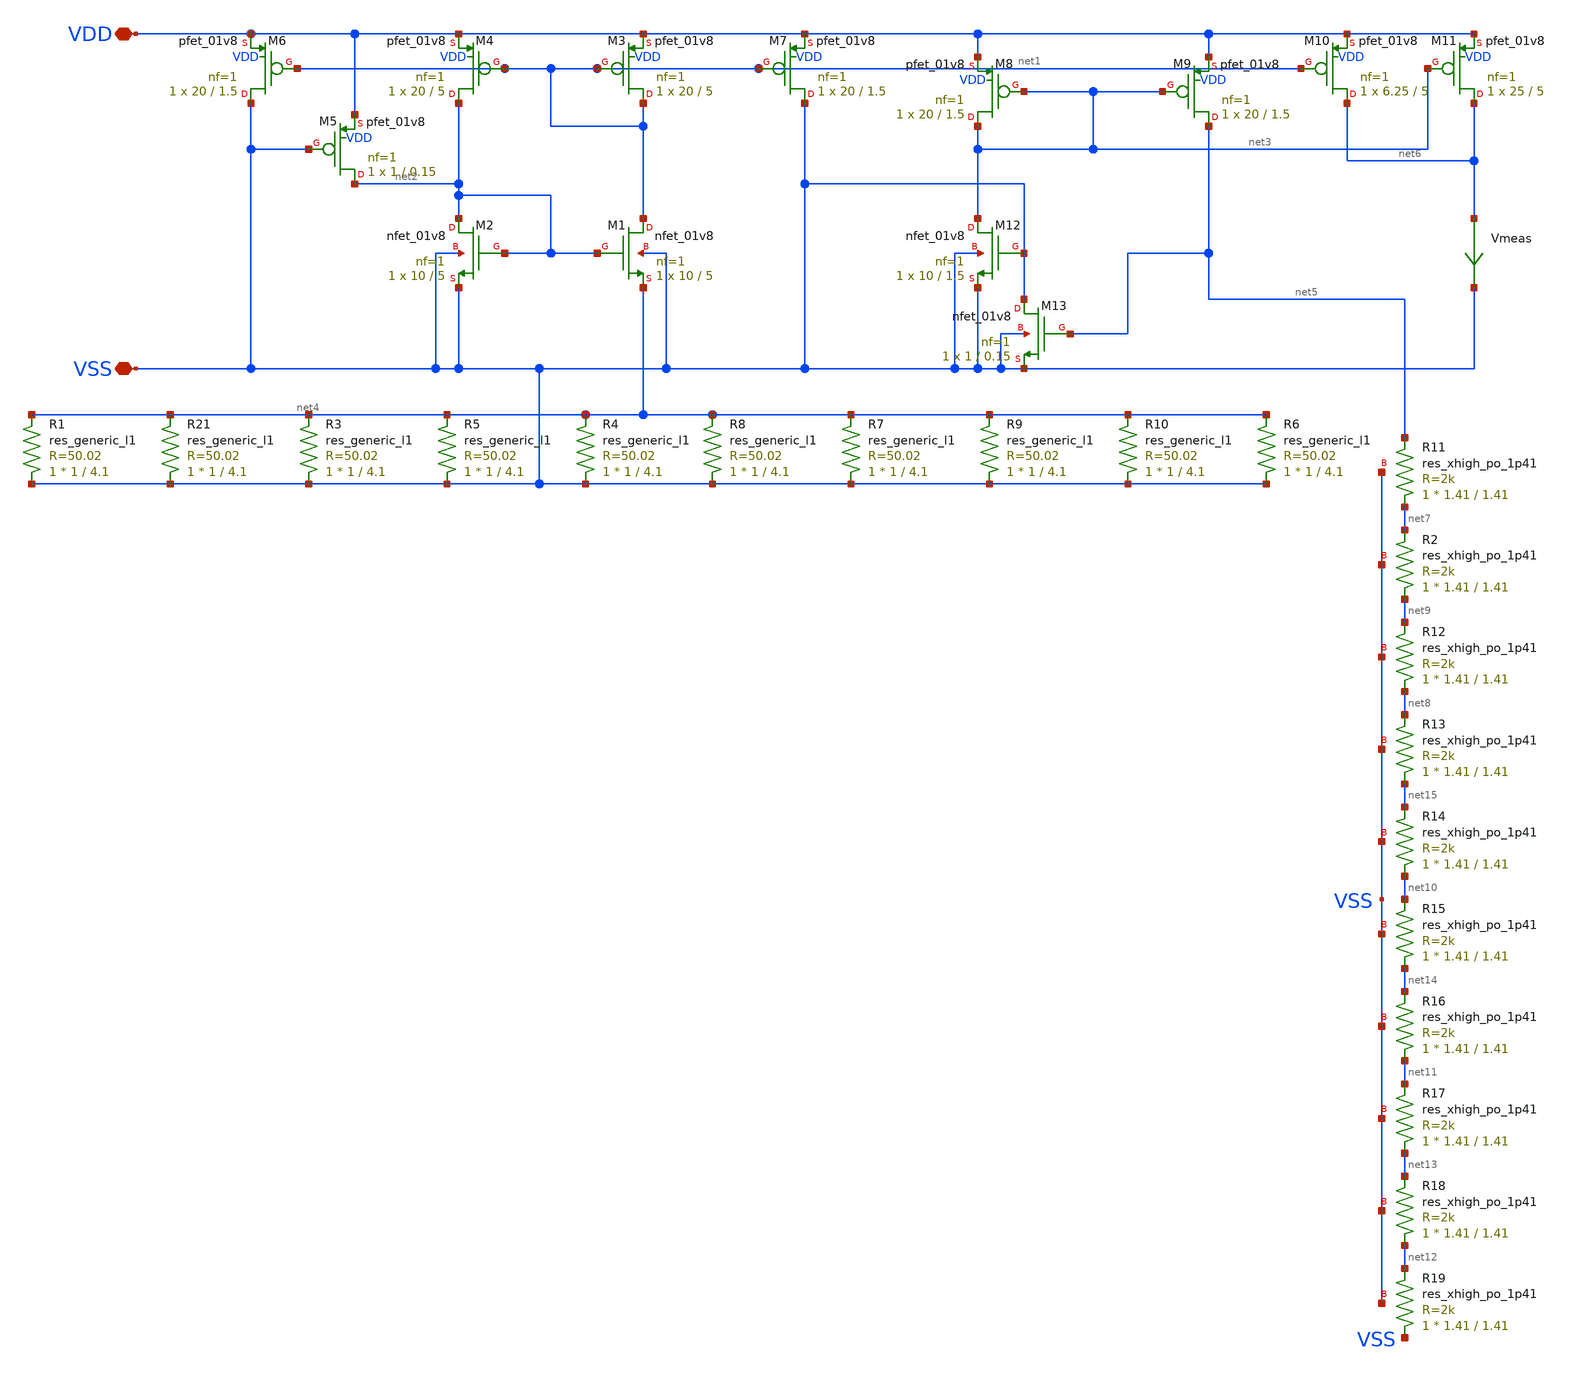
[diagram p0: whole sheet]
** sch_path: bandgap/bgr/current-mode-bgr.sch
**.subckt current-mode-bgr VDD VSS
*.iopin VDD
*.iopin VSS
XM1 net1 net2 net4 VSS sky130_fd_pr__nfet_01v8 L=5 W=10 nf=1 ad='int((nf+1)/2) * W/nf * 0.29' as='int((nf+2)/2) * W/nf * 0.29'
+ pd='2*int((nf+1)/2) * (W/nf + 0.29)' ps='2*int((nf+2)/2) * (W/nf + 0.29)' nrd='0.29 / W' nrs='0.29 / W'
+ sa=0 sb=0 sd=0 mult=1 m=1
XM2 net2 net2 VSS VSS sky130_fd_pr__nfet_01v8 L=5 W=10 nf=1 ad='int((nf+1)/2) * W/nf * 0.29' as='int((nf+2)/2) * W/nf * 0.29'
+ pd='2*int((nf+1)/2) * (W/nf + 0.29)' ps='2*int((nf+2)/2) * (W/nf + 0.29)' nrd='0.29 / W' nrs='0.29 / W'
+ sa=0 sb=0 sd=0 mult=1 m=1
XM3 net1 net1 VDD VDD sky130_fd_pr__pfet_01v8 L=5 W=20 nf=1 ad='int((nf+1)/2) * W/nf * 0.29' as='int((nf+2)/2) * W/nf * 0.29'
+ pd='2*int((nf+1)/2) * (W/nf + 0.29)' ps='2*int((nf+2)/2) * (W/nf + 0.29)' nrd='0.29 / W' nrs='0.29 / W'
+ sa=0 sb=0 sd=0 mult=1 m=1
XM4 net2 net1 VDD VDD sky130_fd_pr__pfet_01v8 L=5 W=20 nf=1 ad='int((nf+1)/2) * W/nf * 0.29' as='int((nf+2)/2) * W/nf * 0.29'
+ pd='2*int((nf+1)/2) * (W/nf + 0.29)' ps='2*int((nf+2)/2) * (W/nf + 0.29)' nrd='0.29 / W' nrs='0.29 / W'
+ sa=0 sb=0 sd=0 mult=1 m=1
XM5 net2 VSS VDD VDD sky130_fd_pr__pfet_01v8 L=0.15 W=1 nf=1 ad='int((nf+1)/2) * W/nf * 0.29' as='int((nf+2)/2) * W/nf * 0.29'
+ pd='2*int((nf+1)/2) * (W/nf + 0.29)' ps='2*int((nf+2)/2) * (W/nf + 0.29)' nrd='0.29 / W' nrs='0.29 / W'
+ sa=0 sb=0 sd=0 mult=1 m=1
XM6 VSS net1 VDD VDD sky130_fd_pr__pfet_01v8 L=1.5 W=20 nf=1 ad='int((nf+1)/2) * W/nf * 0.29' as='int((nf+2)/2) * W/nf * 0.29'
+ pd='2*int((nf+1)/2) * (W/nf + 0.29)' ps='2*int((nf+2)/2) * (W/nf + 0.29)' nrd='0.29 / W' nrs='0.29 / W'
+ sa=0 sb=0 sd=0 mult=1 m=1
XM7 VSS net1 VDD VDD sky130_fd_pr__pfet_01v8 L=1.5 W=20 nf=1 ad='int((nf+1)/2) * W/nf * 0.29' as='int((nf+2)/2) * W/nf * 0.29'
+ pd='2*int((nf+1)/2) * (W/nf + 0.29)' ps='2*int((nf+2)/2) * (W/nf + 0.29)' nrd='0.29 / W' nrs='0.29 / W'
+ sa=0 sb=0 sd=0 mult=1 m=1
XM8 net3 net3 VDD VDD sky130_fd_pr__pfet_01v8 L=1.5 W=20 nf=1 ad='int((nf+1)/2) * W/nf * 0.29' as='int((nf+2)/2) * W/nf * 0.29'
+ pd='2*int((nf+1)/2) * (W/nf + 0.29)' ps='2*int((nf+2)/2) * (W/nf + 0.29)' nrd='0.29 / W' nrs='0.29 / W'
+ sa=0 sb=0 sd=0 mult=1 m=1
XM9 net5 net3 VDD VDD sky130_fd_pr__pfet_01v8 L=1.5 W=20 nf=1 ad='int((nf+1)/2) * W/nf * 0.29' as='int((nf+2)/2) * W/nf * 0.29'
+ pd='2*int((nf+1)/2) * (W/nf + 0.29)' ps='2*int((nf+2)/2) * (W/nf + 0.29)' nrd='0.29 / W' nrs='0.29 / W'
+ sa=0 sb=0 sd=0 mult=1 m=1
XM10 net6 net1 VDD VDD sky130_fd_pr__pfet_01v8 L=5 W=6.25 nf=1 ad='int((nf+1)/2) * W/nf * 0.29' as='int((nf+2)/2) * W/nf * 0.29'
+ pd='2*int((nf+1)/2) * (W/nf + 0.29)' ps='2*int((nf+2)/2) * (W/nf + 0.29)' nrd='0.29 / W' nrs='0.29 / W'
+ sa=0 sb=0 sd=0 mult=1 m=1
XM11 net6 net3 VDD VDD sky130_fd_pr__pfet_01v8 L=5 W=25 nf=1 ad='int((nf+1)/2) * W/nf * 0.29' as='int((nf+2)/2) * W/nf * 0.29'
+ pd='2*int((nf+1)/2) * (W/nf + 0.29)' ps='2*int((nf+2)/2) * (W/nf + 0.29)' nrd='0.29 / W' nrs='0.29 / W'
+ sa=0 sb=0 sd=0 mult=1 m=1
XM12 net3 VSS VSS VSS sky130_fd_pr__nfet_01v8 L=1.5 W=10 nf=1 ad='int((nf+1)/2) * W/nf * 0.29' as='int((nf+2)/2) * W/nf * 0.29'
+ pd='2*int((nf+1)/2) * (W/nf + 0.29)' ps='2*int((nf+2)/2) * (W/nf + 0.29)' nrd='0.29 / W' nrs='0.29 / W'
+ sa=0 sb=0 sd=0 mult=1 m=1
XM13 VSS net5 VSS VSS sky130_fd_pr__nfet_01v8 L=0.15 W=1 nf=1 ad='int((nf+1)/2) * W/nf * 0.29' as='int((nf+2)/2) * W/nf * 0.29'
+ pd='2*int((nf+1)/2) * (W/nf + 0.29)' ps='2*int((nf+2)/2) * (W/nf + 0.29)' nrd='0.29 / W' nrs='0.29 / W'
+ sa=0 sb=0 sd=0 mult=1 m=1
Vmeas net6 VSS 0
.save i(vmeas)
R21 VSS net4 sky130_fd_pr__res_generic_l1 W=1 L=4.1 m=1
R1 VSS net4 sky130_fd_pr__res_generic_l1 W=1 L=4.1 m=1
R3 VSS net4 sky130_fd_pr__res_generic_l1 W=1 L=4.1 m=1
R4 VSS net4 sky130_fd_pr__res_generic_l1 W=1 L=4.1 m=1
R5 VSS net4 sky130_fd_pr__res_generic_l1 W=1 L=4.1 m=1
R6 VSS net4 sky130_fd_pr__res_generic_l1 W=1 L=4.1 m=1
R7 VSS net4 sky130_fd_pr__res_generic_l1 W=1 L=4.1 m=1
R8 VSS net4 sky130_fd_pr__res_generic_l1 W=1 L=4.1 m=1
R9 VSS net4 sky130_fd_pr__res_generic_l1 W=1 L=4.1 m=1
R10 VSS net4 sky130_fd_pr__res_generic_l1 W=1 L=4.1 m=1
XR11 net7 net5 VSS sky130_fd_pr__res_xhigh_po_1p41 L=1.41 mult=1 m=1
XR2 net9 net7 VSS sky130_fd_pr__res_xhigh_po_1p41 L=1.41 mult=1 m=1
XR12 net8 net9 VSS sky130_fd_pr__res_xhigh_po_1p41 L=1.41 mult=1 m=1
XR13 net15 net8 VSS sky130_fd_pr__res_xhigh_po_1p41 L=1.41 mult=1 m=1
XR14 net10 net15 VSS sky130_fd_pr__res_xhigh_po_1p41 L=1.41 mult=1 m=1
XR15 net14 net10 VSS sky130_fd_pr__res_xhigh_po_1p41 L=1.41 mult=1 m=1
XR16 net11 net14 VSS sky130_fd_pr__res_xhigh_po_1p41 L=1.41 mult=1 m=1
XR17 net13 net11 VSS sky130_fd_pr__res_xhigh_po_1p41 L=1.41 mult=1 m=1
XR18 net12 net13 VSS sky130_fd_pr__res_xhigh_po_1p41 L=1.41 mult=1 m=1
XR19 VSS net12 VSS sky130_fd_pr__res_xhigh_po_1p41 L=1.41 mult=1 m=1
**.ends
.end
